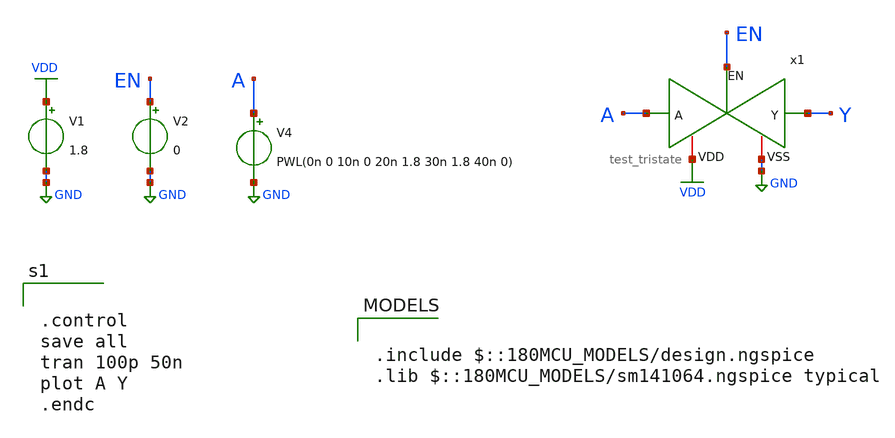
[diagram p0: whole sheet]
** sch_path: designs/libs/tb_test/tb_test_tristate/tb_test_tristate.sch
**.subckt tb_test_tristate
V1 VDD GND 1.8
V2 EN GND 0
x1 VDD EN A Y GND test_tristate
V4 A GND PWL(0n 0 10n 0 20n 1.8 30n 1.8 40n 0)
**** begin user architecture code

.include $::180MCU_MODELS/design.ngspice
.lib $::180MCU_MODELS/sm141064.ngspice typical



.control
save all
tran 100p 50n
plot A Y
.endc


**** end user architecture code
**.ends
.GLOBAL GND
.GLOBAL VDD
.end
